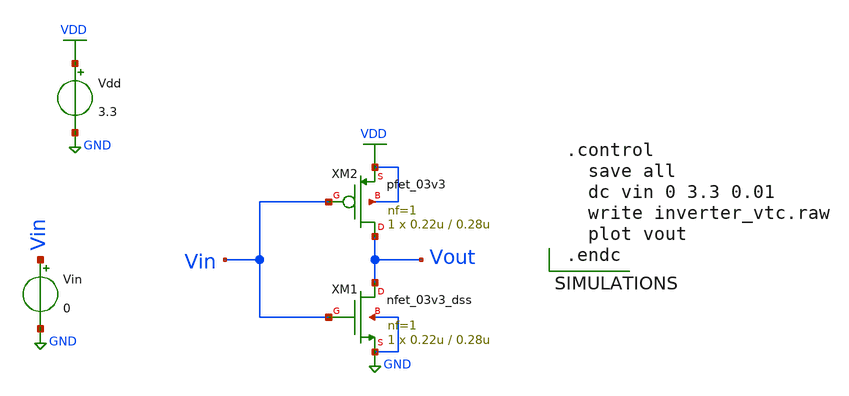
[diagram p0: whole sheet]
** sch_path: OR/inverter_vtc.sch
**.subckt inverter_vtc
XM1 Vout Vin GND GND nfet_03v3_dss L=0.28u W=0.22u nf=1 ad='int((nf+1)/2) * W/nf * 0.18u' as='int((nf+2)/2) * W/nf * 0.18u'
+ pd='2*int((nf+1)/2) * (W/nf + 0.18u)' ps='2*int((nf+2)/2) * (W/nf + 0.18u)' nrd='0.18u / W' nrs='0.18u / W'
+ sa=0 sb=0 sd=0 m=1
XM2 Vout Vin VDD VDD pfet_03v3 L=0.28u W=0.22u nf=1 ad='int((nf+1)/2) * W/nf * 0.18u' as='int((nf+2)/2) * W/nf * 0.18u'
+ pd='2*int((nf+1)/2) * (W/nf + 0.18u)' ps='2*int((nf+2)/2) * (W/nf + 0.18u)' nrd='0.18u / W' nrs='0.18u / W'
+ sa=0 sb=0 sd=0 m=1
Vdd VDD GND 3.3
Vin Vin GND 0
**** begin user architecture code


.control
  save all
  dc vin 0 3.3 0.01
  write inverter_vtc.raw
  plot vout
.endc




.include /foss/pdks/gf180mcuD/libs.tech/ngspice/design.ngspice
.lib /foss/pdks/gf180mcuD/libs.tech/ngspice/sm141064.ngspice typical


**** end user architecture code
**.ends
.GLOBAL VDD
.GLOBAL GND
.end
